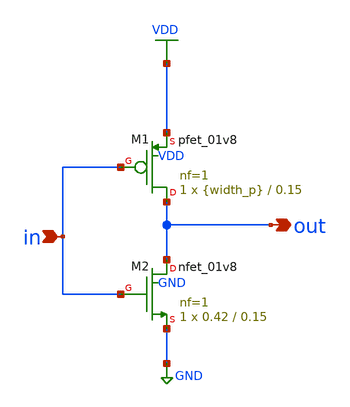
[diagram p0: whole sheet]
** sch_path: tutorial-3/source/q1.sch
**.subckt q1 in out
*.ipin in
*.opin out
XM1 out in VDD VDD sky130_fd_pr__pfet_01v8 L=0.15 W={width_p} nf=1 ad='int((nf+1)/2) * W/nf * 0.29' as='int((nf+2)/2) * W/nf * 0.29'
+ pd='2*int((nf+1)/2) * (W/nf + 0.29)' ps='2*int((nf+2)/2) * (W/nf + 0.29)' nrd='0.29 / W' nrs='0.29 / W'
+ sa=0 sb=0 sd=0 mult=1 m=1
XM2 out in GND GND sky130_fd_pr__nfet_01v8 L=0.15 W=0.42 nf=1 ad='int((nf+1)/2) * W/nf * 0.29' as='int((nf+2)/2) * W/nf * 0.29'
+ pd='2*int((nf+1)/2) * (W/nf + 0.29)' ps='2*int((nf+2)/2) * (W/nf + 0.29)' nrd='0.29 / W' nrs='0.29 / W'
+ sa=0 sb=0 sd=0 mult=1 m=1
**.ends
.GLOBAL VDD
.GLOBAL GND
.end
